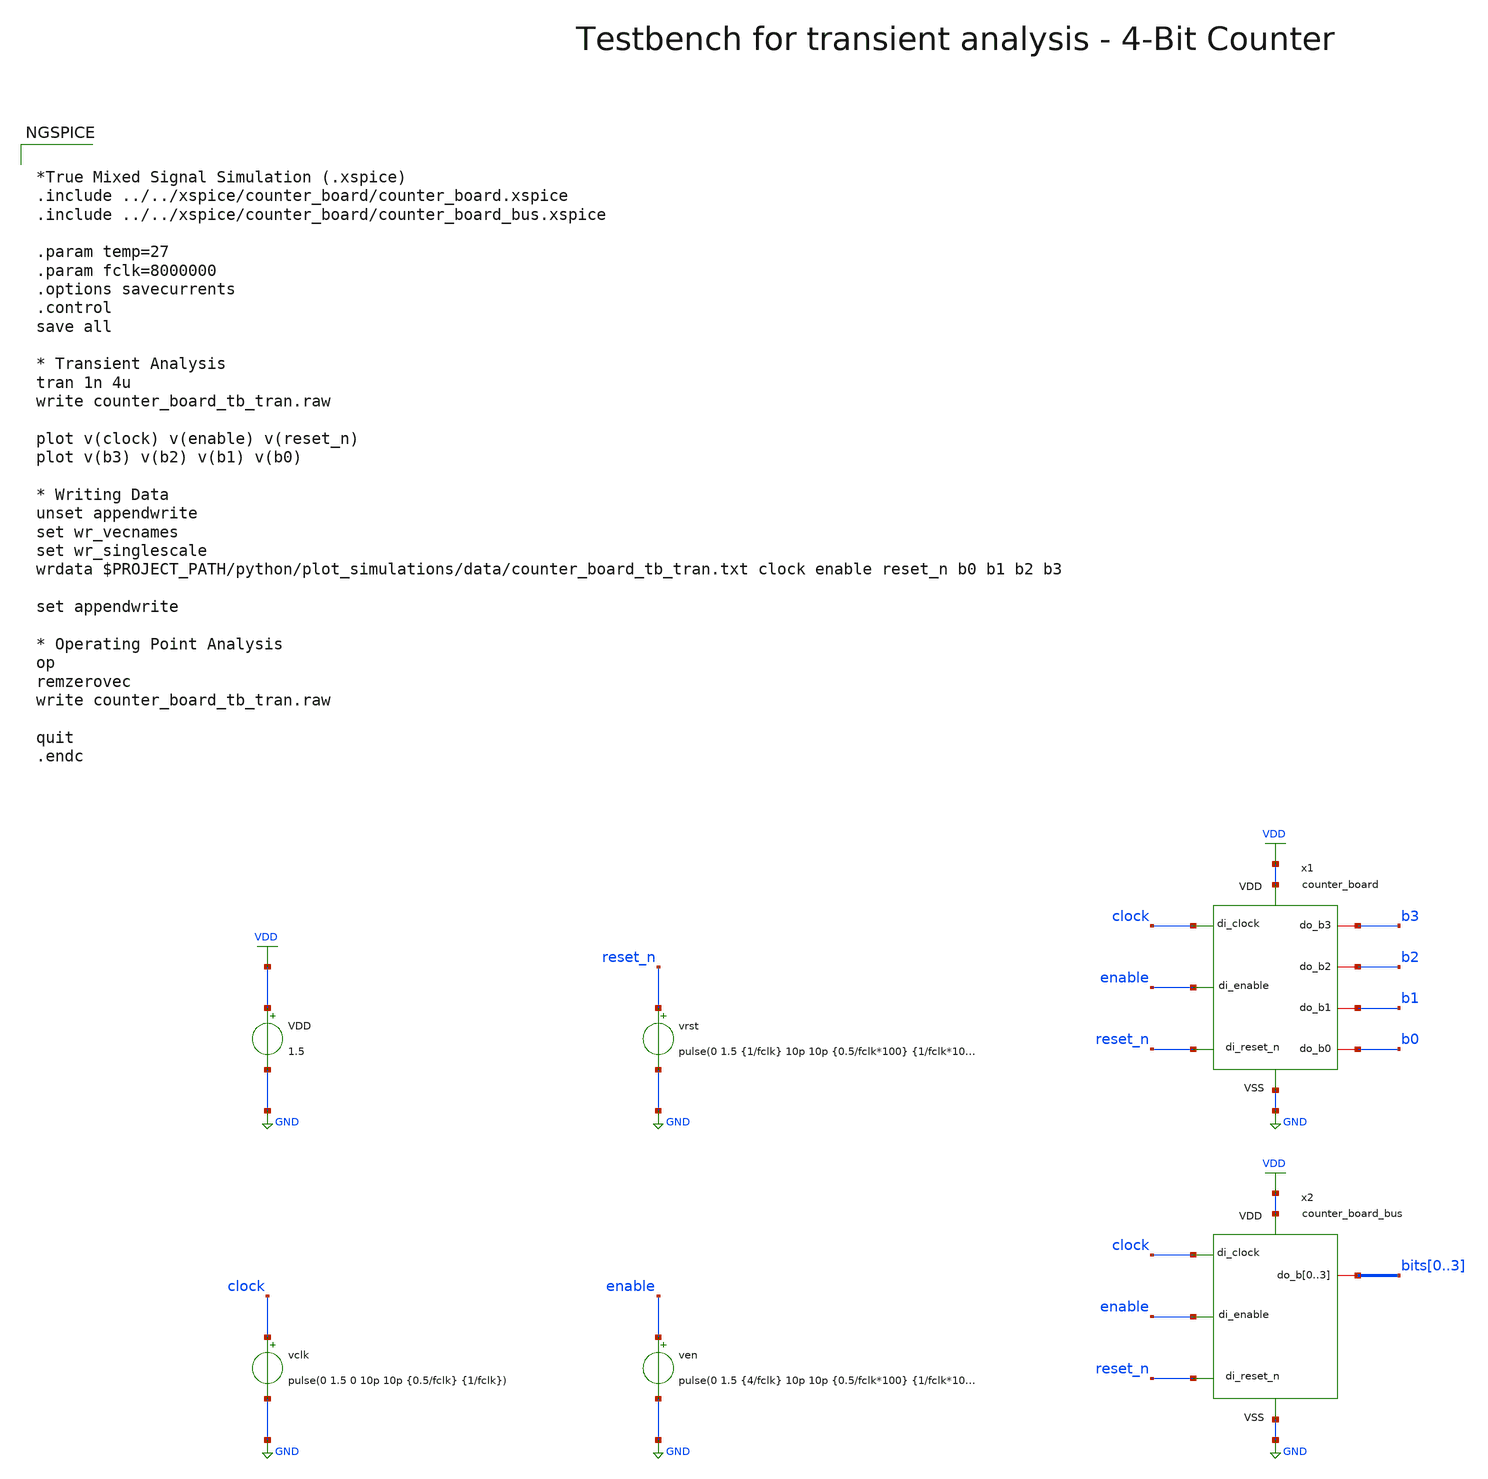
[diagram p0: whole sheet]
** sch_path: xschem/testbenches/counter_board_tb_tran.sch
**.subckt counter_board_tb_tran
VDD VDD GND 1.5
vclk clock GND pulse(0 1.5 0 10p 10p {0.5/fclk} {1/fclk})
vrst reset_n GND pulse(0 1.5 {1/fclk} 10p 10p {0.5/fclk*100} {1/fclk*100})
ven enable GND pulse(0 1.5 {4/fclk} 10p 10p {0.5/fclk*100} {1/fclk*100})
x1 VDD GND clock reset_n enable b0 b1 b2 b3 counter_board
x2 VDD GND clock reset_n enable bits0 bits1 bits2 bits3 counter_board_bus
**** begin user architecture code


*True Mixed Signal Simulation (.xspice)
.include ../../xspice/counter_board/counter_board.xspice
.include ../../xspice/counter_board/counter_board_bus.xspice

.param temp=27
.param fclk=8000000
.options savecurrents
.control
save all

* Transient Analysis
tran 1n 4u
write counter_board_tb_tran.raw

plot v(clock) v(enable) v(reset_n)
plot v(b3) v(b2) v(b1) v(b0)

* Writing Data
unset appendwrite
set wr_vecnames
set wr_singlescale
wrdata $PROJECT_PATH/python/plot_simulations/data/counter_board_tb_tran.txt clock enable reset_n b0
+ b1 b2 b3

set appendwrite

* Operating Point Analysis
op
remzerovec
write counter_board_tb_tran.raw

quit
.endc


.lib cornerMOSlv.lib mos_tt
.lib cornerMOShv.lib mos_tt
.lib cornerHBT.lib hbt_typ
.lib cornerRES.lib res_typ
.lib cornerDIO.lib dio_tt

**** end user architecture code
**.ends
.GLOBAL GND
.GLOBAL VDD
.end
